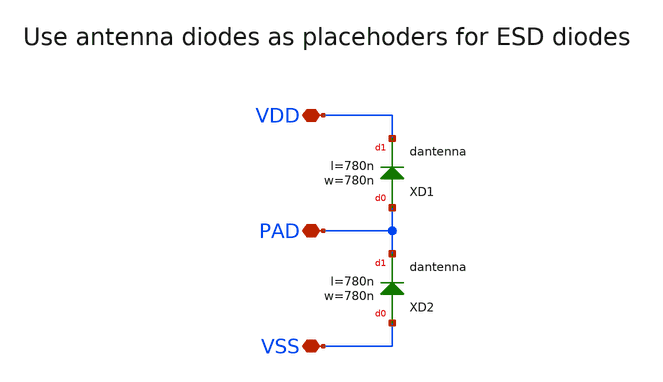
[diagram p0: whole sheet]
** sch_path: JKU_TC1/design_data/xschem/pads/pad_diodes.sch
**.subckt pad_diodes VDD VSS PAD
*.iopin VDD
*.iopin VSS
*.iopin PAD
XXD1 PAD VDD dantenna l=780n w=780n
XXD2 VSS PAD dantenna l=780n w=780n
**.ends
.end
